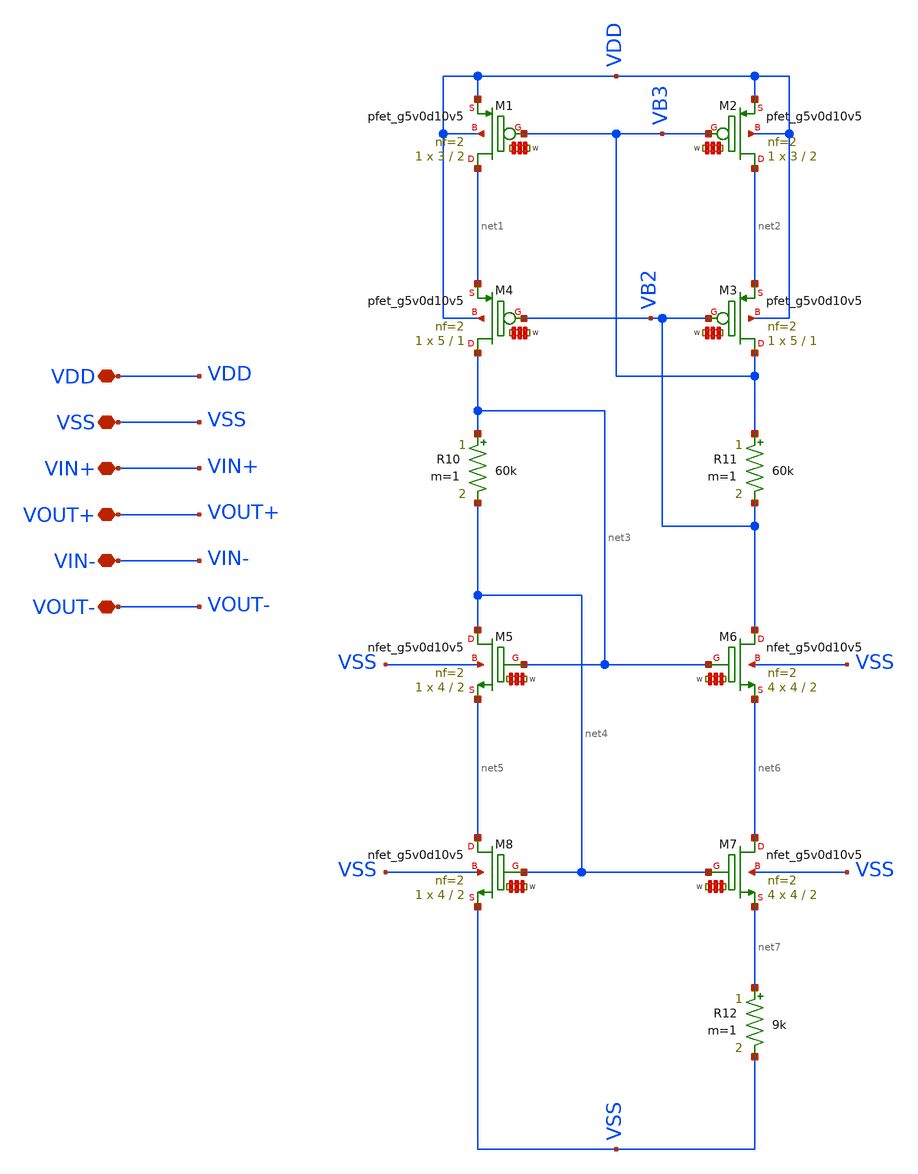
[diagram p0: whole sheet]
** sch_path: my_ip/sky130A/fully_differential_telescopic_cascode_5V_V1/fd_opamp.sch
**.subckt fd_opamp VDD VSS VIN+ VOUT+ VIN- VOUT-
*.iopin VDD
*.iopin VSS
*.iopin VIN+
*.iopin VOUT+
*.iopin VIN-
*.iopin VOUT-
XM1 net1 VB3 VDD VDD sky130_fd_pr__pfet_g5v0d10v5 L=2 W='3 * 2 ' nf=2 ad='int((2 + 1)/2) * 3 * 0.29'
+ as='int((2 + 2)/2) * 3 * 0.29' pd='2*int((2 + 1)/2) * (3 + 0.29)' ps='2*int((2 + 2)/2) * (3 + 0.29)'
+ nrd='0.29 / 3 / 2 ' nrs='0.29 / 3 / 2 ' sa=0 sb=0 sd=0 mult=1 m=1
XM3 VB3 VB2 net2 VDD sky130_fd_pr__pfet_g5v0d10v5 L=1 W='5 * 2 ' nf=2 ad='int((2 + 1)/2) * 5 * 0.29'
+ as='int((2 + 2)/2) * 5 * 0.29' pd='2*int((2 + 1)/2) * (5 + 0.29)' ps='2*int((2 + 2)/2) * (5 + 0.29)'
+ nrd='0.29 / 5 / 2 ' nrs='0.29 / 5 / 2 ' sa=0 sb=0 sd=0 mult=1 m=1
R10 net3 net4 60k m=1
R11 VB3 VB2 60k m=1
XM7 net6 net4 net7 VSS sky130_fd_pr__nfet_g5v0d10v5 L=2 W='4 * 2 ' nf=2 ad='int((nf+1)/2) * W / nf * 0.29'
+ as='int((nf+2)/2) * W / nf * 0.29' pd='2*int((nf+1)/2) * (W / nf + 0.29)' ps='2*int((nf+2)/2) * (W / nf + 0.29)'
+ nrd='0.29 / W ' nrs='0.29 / W ' sa=0 sb=0 sd=0 mult=4 m=4
R12 net7 VSS 9k m=1
XM2 net2 VB3 VDD VDD sky130_fd_pr__pfet_g5v0d10v5 L=2 W='3 * 2 ' nf=2 ad='int((2 + 1)/2) * 3 * 0.29'
+ as='int((2 + 2)/2) * 3 * 0.29' pd='2*int((2 + 1)/2) * (3 + 0.29)' ps='2*int((2 + 2)/2) * (3 + 0.29)'
+ nrd='0.29 / 3 / 2 ' nrs='0.29 / 3 / 2 ' sa=0 sb=0 sd=0 mult=1 m=1
XM6 VB2 net3 net6 VSS sky130_fd_pr__nfet_g5v0d10v5 L=2 W='4 * 2 ' nf=2 ad='int((nf+1)/2) * W / nf * 0.29'
+ as='int((nf+2)/2) * W / nf * 0.29' pd='2*int((nf+1)/2) * (W / nf + 0.29)' ps='2*int((nf+2)/2) * (W / nf + 0.29)'
+ nrd='0.29 / W ' nrs='0.29 / W ' sa=0 sb=0 sd=0 mult=4 m=4
XM5 net4 net3 net5 VSS sky130_fd_pr__nfet_g5v0d10v5 L=2 W='4 * 2 ' nf=2 ad='int((nf+1)/2) * W / nf * 0.29'
+ as='int((nf+2)/2) * W / nf * 0.29' pd='2*int((nf+1)/2) * (W / nf + 0.29)' ps='2*int((nf+2)/2) * (W / nf + 0.29)'
+ nrd='0.29 / W ' nrs='0.29 / W ' sa=0 sb=0 sd=0 mult=1 m=1
XM8 net5 net4 VSS VSS sky130_fd_pr__nfet_g5v0d10v5 L=2 W='4 * 2 ' nf=2 ad='int((nf+1)/2) * W / nf * 0.29'
+ as='int((nf+2)/2) * W / nf * 0.29' pd='2*int((nf+1)/2) * (W / nf + 0.29)' ps='2*int((nf+2)/2) * (W / nf + 0.29)'
+ nrd='0.29 / W ' nrs='0.29 / W ' sa=0 sb=0 sd=0 mult=1 m=1
XM4 net3 VB2 net1 VDD sky130_fd_pr__pfet_g5v0d10v5 L=1 W='5 * 2 ' nf=2 ad='int((2 + 1)/2) * 5 * 0.29'
+ as='int((2 + 2)/2) * 5 * 0.29' pd='2*int((2 + 1)/2) * (5 + 0.29)' ps='2*int((2 + 2)/2) * (5 + 0.29)'
+ nrd='0.29 / 5 / 2 ' nrs='0.29 / 5 / 2 ' sa=0 sb=0 sd=0 mult=1 m=1
**.ends
.end
